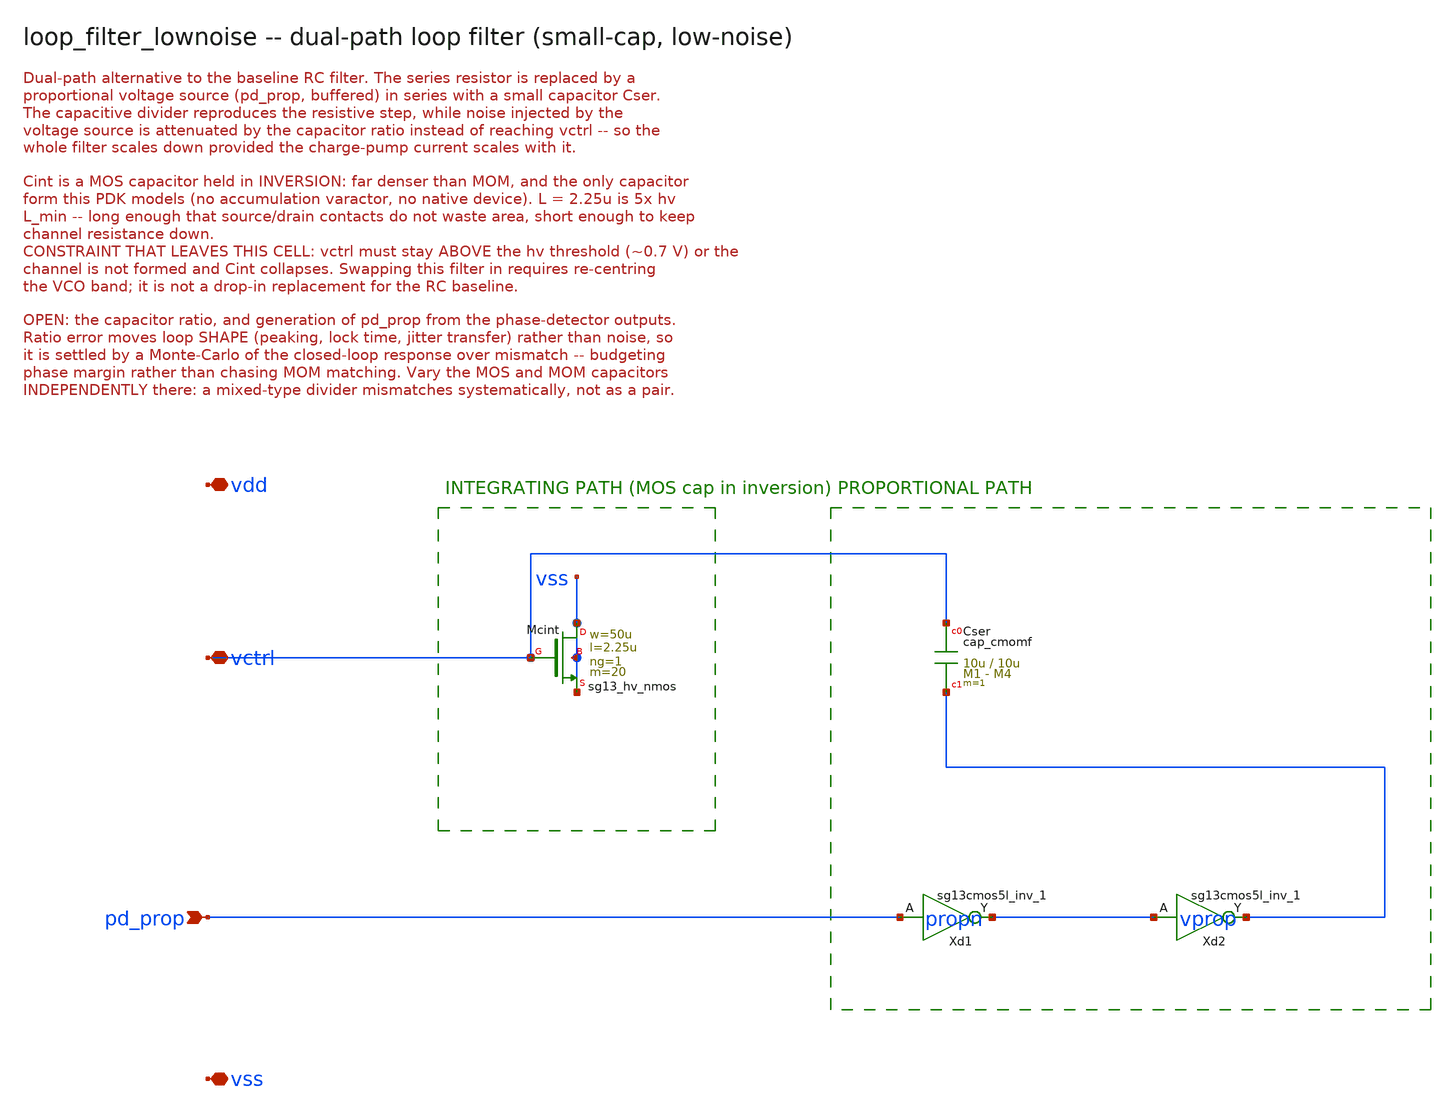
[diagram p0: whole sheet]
** sch_path: xschem/loop_filter_lownoise_wired.sch
**.subckt loop_filter_lownoise_wired vctrl pd_prop vdd vss
*.iopin vctrl
*.ipin pd_prop
*.iopin vdd
*.iopin vss
XMcint vss vctrl vss vss sg13_hv_nmos w=50u l=2.25u ng=1 m=20 mm_ok=1
XCser vctrl vprop cap_cmomf w=10u l=10u mmin=1 mmax=4 subblock=0 rfmodel=0 subscale=1 m=1 mm_ok=1
Xd1 propn pd_prop vdd vss sg13cmos5l_inv_1
Xd2 vprop propn vdd vss sg13cmos5l_inv_1
**.ends
.end
